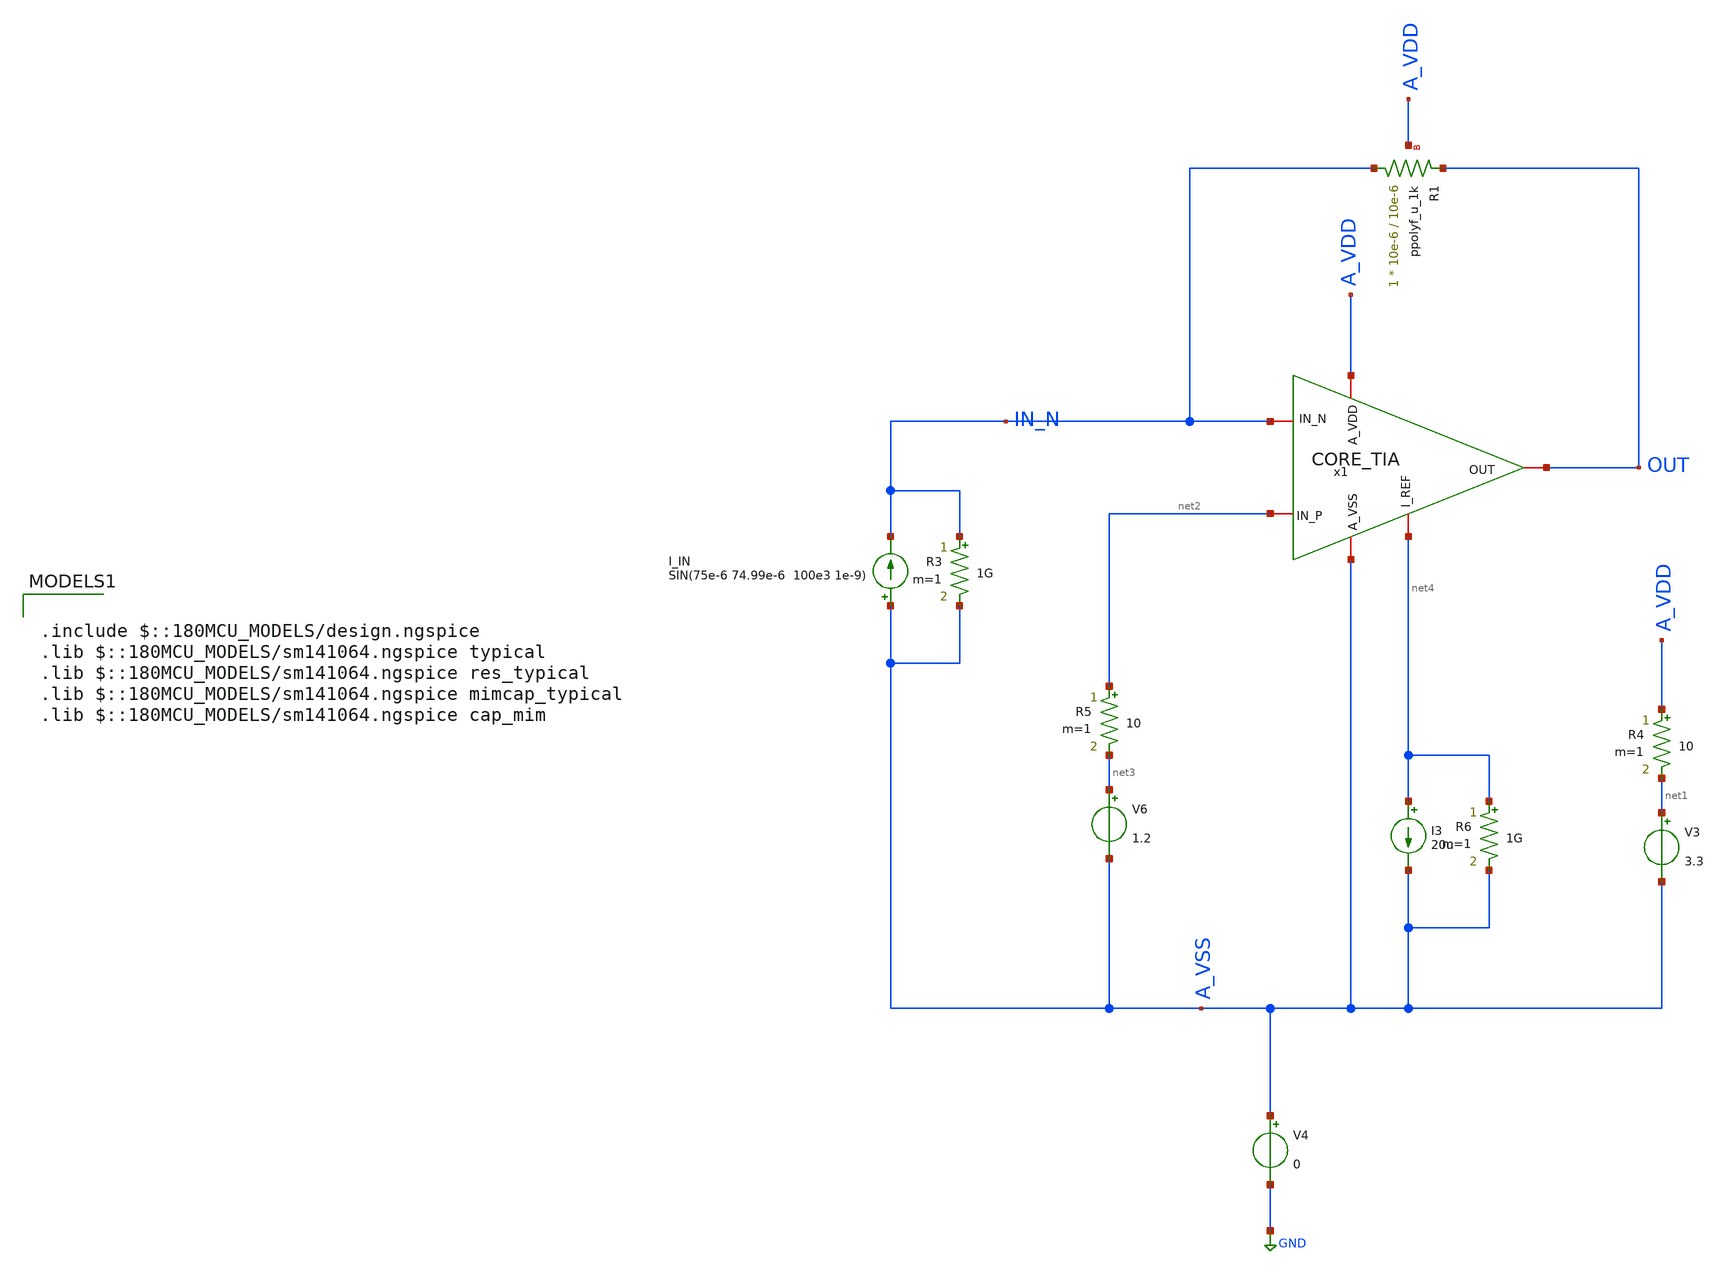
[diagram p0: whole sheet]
** sch_path: designs/libs/TIA/TB_CORE_TRAN_LINEARITY.sch
**.subckt TB_CORE_TRAN_LINEARITY
x1 A_VDD A_VSS IN_N net2 net4 OUT CORE_TIA
V3 net1 A_VSS 3.3
V4 A_VSS GND 0
V6 net3 A_VSS 1.2
I3 net4 A_VSS 20u
I_IN A_VSS IN_N SIN(75e-6 74.99e-6 100e3 1e-9)
R3 IN_N A_VSS 1G m=1
R4 A_VDD net1 10 m=1
R5 net2 net3 10 m=1
R6 net4 A_VSS 1G m=1
XR1 IN_N OUT A_VDD ppolyf_u_1k r_width=10e-6 r_length=10e-6 m=1
**** begin user architecture code

.include $::180MCU_MODELS/design.ngspice
.lib $::180MCU_MODELS/sm141064.ngspice typical
.lib $::180MCU_MODELS/sm141064.ngspice res_typical
.lib $::180MCU_MODELS/sm141064.ngspice mimcap_typical
.lib $::180MCU_MODELS/sm141064.ngspice cap_mim




.control
save all


** Simulation

let tstop = 60e-6
let tstep = 1e-9

op

tran $&tstep $&tstop

dc I_IN 200e-9 300e-6 10e-9


** Plots

setplot tran1
let v_out = v(OUT)

let i_in = -(v(OUT)-v(IN_N))/1e3

plot v_out

plot i_in

write TB_CORE_TRAN.raw


setplot dc1

let v_out = v(OUT)

let i_in = -(v(OUT)-v(IN_N))/1e3

plot v_out

plot i_in




write TB_CORE_LINEARITY.raw




.endc


**** end user architecture code
**.ends
.GLOBAL GND
.end
